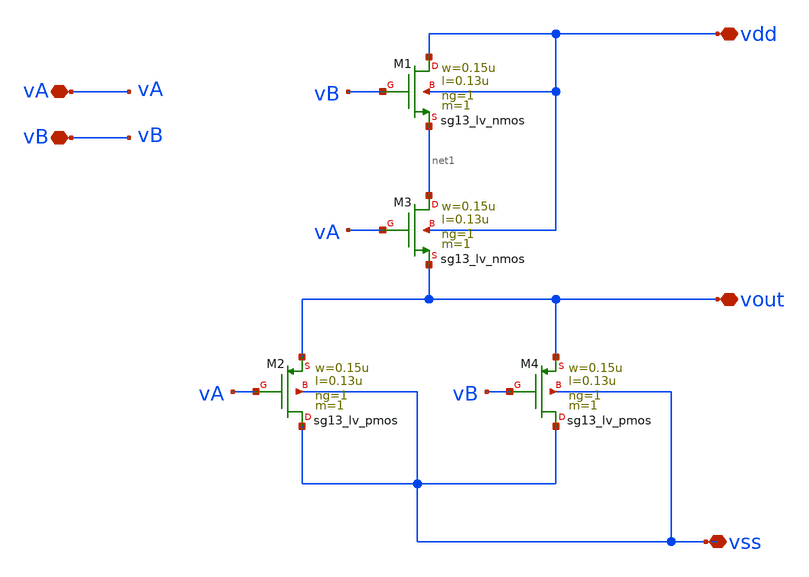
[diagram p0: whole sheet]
** sch_path: design/blocks/norgate/schematic/norgate.sch
**.subckt norgate vout vdd vss vA vB
*.iopin vout
*.iopin vdd
*.iopin vss
*.iopin vA
*.iopin vB
XM1 vdd vB net1 vdd sg13_lv_nmos w=0.15u l=0.13u ng=1 m=1 mm_ok=1
XM2 vss vA vout vss sg13_lv_pmos w=0.15u l=0.13u ng=1 m=1 mm_ok=1
XM3 net1 vA vout vdd sg13_lv_nmos w=0.15u l=0.13u ng=1 m=1 mm_ok=1
XM4 vss vB vout vss sg13_lv_pmos w=0.15u l=0.13u ng=1 m=1 mm_ok=1
**.ends
.end
